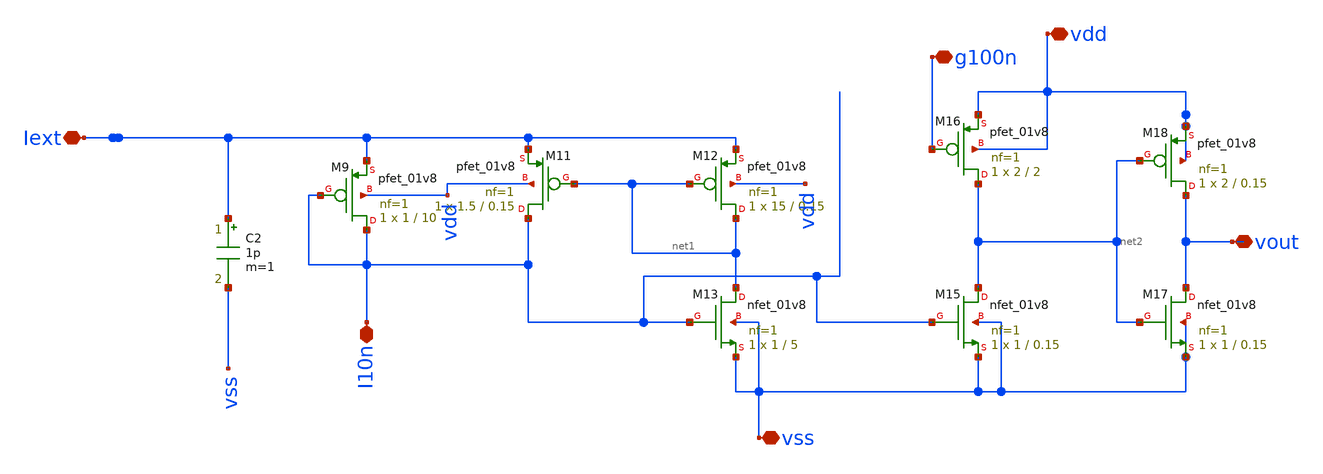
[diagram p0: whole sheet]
** sch_path: Neuron/ultralif/ultra_post.sch
**.subckt ultra_post Iext vout vss I10n vdd g100n
*.iopin Iext
*.iopin vout
*.iopin vss
*.iopin I10n
*.iopin vdd
*.iopin g100n
XM9 I10n I10n Iext vdd sky130_fd_pr__pfet_01v8 L=10 W=1 nf=1 ad='int((nf+1)/2) * W/nf * 0.29' as='int((nf+2)/2) * W/nf * 0.29'
+ pd='2*int((nf+1)/2) * (W/nf + 0.29)' ps='2*int((nf+2)/2) * (W/nf + 0.29)' nrd='0.29 / W' nrs='0.29 / W'
+ sa=0 sb=0 sd=0 mult=1 m=1
XM11 I10n net1 Iext vdd sky130_fd_pr__pfet_01v8 L=0.15 W=1.5 nf=1 ad='int((nf+1)/2) * W/nf * 0.29' as='int((nf+2)/2) * W/nf * 0.29'
+ pd='2*int((nf+1)/2) * (W/nf + 0.29)' ps='2*int((nf+2)/2) * (W/nf + 0.29)' nrd='0.29 / W' nrs='0.29 / W'
+ sa=0 sb=0 sd=0 mult=1 m=1
XM12 net1 net1 Iext vdd sky130_fd_pr__pfet_01v8 L=0.15 W=15 nf=1 ad='int((nf+1)/2) * W/nf * 0.29' as='int((nf+2)/2) * W/nf * 0.29'
+ pd='2*int((nf+1)/2) * (W/nf + 0.29)' ps='2*int((nf+2)/2) * (W/nf + 0.29)' nrd='0.29 / W' nrs='0.29 / W'
+ sa=0 sb=0 sd=0 mult=1 m=1
XM13 net1 I10n vss vss sky130_fd_pr__nfet_01v8 L=5 W=1 nf=1 ad='int((1 + 1)/2) * 1 / 1 * 0.29' as='int((1 + 2)/2) * 1 / 1 * 0.29'
+ pd='2*int((1 + 1)/2) * (1 / 1 + 0.29)' ps='2*int((1 + 2)/2) * (1 / 1 + 0.29)' nrd='0.29 / 1 ' nrs='0.29 / 1 '
+ sa=0 sb=0 sd=0 mult=1 m=1
C2 Iext vss 1p m=1
XM15 net2 I10n vss vss sky130_fd_pr__nfet_01v8 L=0.15 W=1 nf=1 ad='int((1 + 1)/2) * 1 / 1 * 0.29' as='int((1 + 2)/2) * 1 / 1 * 0.29'
+ pd='2*int((1 + 1)/2) * (1 / 1 + 0.29)' ps='2*int((1 + 2)/2) * (1 / 1 + 0.29)' nrd='0.29 / 1 ' nrs='0.29 / 1 '
+ sa=0 sb=0 sd=0 mult=1 m=1
XM16 net2 g100n vdd vdd sky130_fd_pr__pfet_01v8 L=2 W=2 nf=1 ad='int((nf+1)/2) * W/nf * 0.29' as='int((nf+2)/2) * W/nf * 0.29'
+ pd='2*int((nf+1)/2) * (W/nf + 0.29)' ps='2*int((nf+2)/2) * (W/nf + 0.29)' nrd='0.29 / W' nrs='0.29 / W'
+ sa=0 sb=0 sd=0 mult=1 m=1
XM17 vout net2 vss vss sky130_fd_pr__nfet_01v8 L=0.15 W=1 nf=1 ad='int((1 + 1)/2) * 1 / 1 * 0.29' as='int((1 + 2)/2) * 1 / 1 * 0.29'
+ pd='2*int((1 + 1)/2) * (1 / 1 + 0.29)' ps='2*int((1 + 2)/2) * (1 / 1 + 0.29)' nrd='0.29 / 1 ' nrs='0.29 / 1 '
+ sa=0 sb=0 sd=0 mult=1 m=1
XM18 vout net2 vdd vdd sky130_fd_pr__pfet_01v8 L=0.15 W=2 nf=1 ad='int((nf+1)/2) * W/nf * 0.29' as='int((nf+2)/2) * W/nf * 0.29'
+ pd='2*int((nf+1)/2) * (W/nf + 0.29)' ps='2*int((nf+2)/2) * (W/nf + 0.29)' nrd='0.29 / W' nrs='0.29 / W'
+ sa=0 sb=0 sd=0 mult=1 m=1
**.ends
.end
